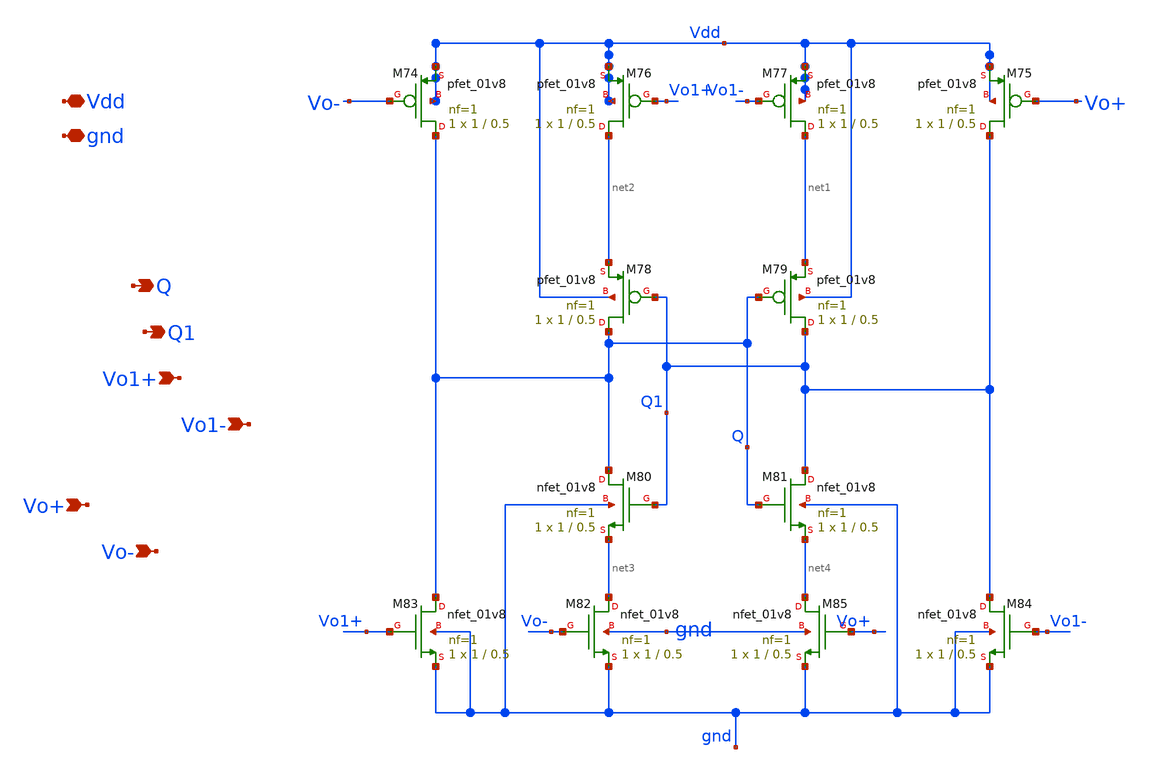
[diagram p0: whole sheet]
** sch_path: xschem/latch_lvs.sch
**.subckt latch_lvs gnd Vdd Q Q1 Vo+ Vo- Vo1+ Vo1-
*.iopin gnd
*.iopin Vdd
*.opin Q
*.opin Q1
*.ipin Vo+
*.ipin Vo-
*.ipin Vo1+
*.ipin Vo1-
XM74 Q Vo- Vdd Vdd sky130_fd_pr__pfet_01v8 L=0.5 W=1 nf=1 ad='int((nf+1)/2) * W/nf * 0.29' as='int((nf+2)/2) * W/nf * 0.29'
+ pd='2*int((nf+1)/2) * (W/nf + 0.29)' ps='2*int((nf+2)/2) * (W/nf + 0.29)' nrd='0.29 / W' nrs='0.29 / W'
+ sa=0 sb=0 sd=0 mult=1 m=1
XM75 Q1 Vo+ Vdd Vdd sky130_fd_pr__pfet_01v8 L=0.5 W=1 nf=1 ad='int((nf+1)/2) * W/nf * 0.29' as='int((nf+2)/2) * W/nf * 0.29'
+ pd='2*int((nf+1)/2) * (W/nf + 0.29)' ps='2*int((nf+2)/2) * (W/nf + 0.29)' nrd='0.29 / W' nrs='0.29 / W'
+ sa=0 sb=0 sd=0 mult=1 m=1
XM76 net2 Vo1+ Vdd Vdd sky130_fd_pr__pfet_01v8 L=0.5 W=1 nf=1 ad='int((nf+1)/2) * W/nf * 0.29' as='int((nf+2)/2) * W/nf * 0.29'
+ pd='2*int((nf+1)/2) * (W/nf + 0.29)' ps='2*int((nf+2)/2) * (W/nf + 0.29)' nrd='0.29 / W' nrs='0.29 / W'
+ sa=0 sb=0 sd=0 mult=1 m=1
XM77 net1 Vo1- Vdd Vdd sky130_fd_pr__pfet_01v8 L=0.5 W=1 nf=1 ad='int((nf+1)/2) * W/nf * 0.29' as='int((nf+2)/2) * W/nf * 0.29'
+ pd='2*int((nf+1)/2) * (W/nf + 0.29)' ps='2*int((nf+2)/2) * (W/nf + 0.29)' nrd='0.29 / W' nrs='0.29 / W'
+ sa=0 sb=0 sd=0 mult=1 m=1
XM78 Q Q1 net2 Vdd sky130_fd_pr__pfet_01v8 L=0.5 W=1 nf=1 ad='int((nf+1)/2) * W/nf * 0.29' as='int((nf+2)/2) * W/nf * 0.29'
+ pd='2*int((nf+1)/2) * (W/nf + 0.29)' ps='2*int((nf+2)/2) * (W/nf + 0.29)' nrd='0.29 / W' nrs='0.29 / W'
+ sa=0 sb=0 sd=0 mult=1 m=1
XM79 Q1 Q net1 Vdd sky130_fd_pr__pfet_01v8 L=0.5 W=1 nf=1 ad='int((nf+1)/2) * W/nf * 0.29' as='int((nf+2)/2) * W/nf * 0.29'
+ pd='2*int((nf+1)/2) * (W/nf + 0.29)' ps='2*int((nf+2)/2) * (W/nf + 0.29)' nrd='0.29 / W' nrs='0.29 / W'
+ sa=0 sb=0 sd=0 mult=1 m=1
XM80 Q Q1 net3 gnd sky130_fd_pr__nfet_01v8 L=0.5 W=1 nf=1 ad='int((nf+1)/2) * W/nf * 0.29' as='int((nf+2)/2) * W/nf * 0.29'
+ pd='2*int((nf+1)/2) * (W/nf + 0.29)' ps='2*int((nf+2)/2) * (W/nf + 0.29)' nrd='0.29 / W' nrs='0.29 / W'
+ sa=0 sb=0 sd=0 mult=1 m=1
XM81 Q1 Q net4 gnd sky130_fd_pr__nfet_01v8 L=0.5 W=1 nf=1 ad='int((nf+1)/2) * W/nf * 0.29' as='int((nf+2)/2) * W/nf * 0.29'
+ pd='2*int((nf+1)/2) * (W/nf + 0.29)' ps='2*int((nf+2)/2) * (W/nf + 0.29)' nrd='0.29 / W' nrs='0.29 / W'
+ sa=0 sb=0 sd=0 mult=1 m=1
XM82 net3 Vo- gnd gnd sky130_fd_pr__nfet_01v8 L=0.5 W=1 nf=1 ad='int((nf+1)/2) * W/nf * 0.29' as='int((nf+2)/2) * W/nf * 0.29'
+ pd='2*int((nf+1)/2) * (W/nf + 0.29)' ps='2*int((nf+2)/2) * (W/nf + 0.29)' nrd='0.29 / W' nrs='0.29 / W'
+ sa=0 sb=0 sd=0 mult=1 m=1
XM83 Q Vo1+ gnd gnd sky130_fd_pr__nfet_01v8 L=0.5 W=1 nf=1 ad='int((nf+1)/2) * W/nf * 0.29' as='int((nf+2)/2) * W/nf * 0.29'
+ pd='2*int((nf+1)/2) * (W/nf + 0.29)' ps='2*int((nf+2)/2) * (W/nf + 0.29)' nrd='0.29 / W' nrs='0.29 / W'
+ sa=0 sb=0 sd=0 mult=1 m=1
XM84 Q1 Vo1- gnd gnd sky130_fd_pr__nfet_01v8 L=0.5 W=1 nf=1 ad='int((nf+1)/2) * W/nf * 0.29' as='int((nf+2)/2) * W/nf * 0.29'
+ pd='2*int((nf+1)/2) * (W/nf + 0.29)' ps='2*int((nf+2)/2) * (W/nf + 0.29)' nrd='0.29 / W' nrs='0.29 / W'
+ sa=0 sb=0 sd=0 mult=1 m=1
XM85 net4 Vo+ gnd gnd sky130_fd_pr__nfet_01v8 L=0.5 W=1 nf=1 ad='int((nf+1)/2) * W/nf * 0.29' as='int((nf+2)/2) * W/nf * 0.29'
+ pd='2*int((nf+1)/2) * (W/nf + 0.29)' ps='2*int((nf+2)/2) * (W/nf + 0.29)' nrd='0.29 / W' nrs='0.29 / W'
+ sa=0 sb=0 sd=0 mult=1 m=1
**.ends
.end
